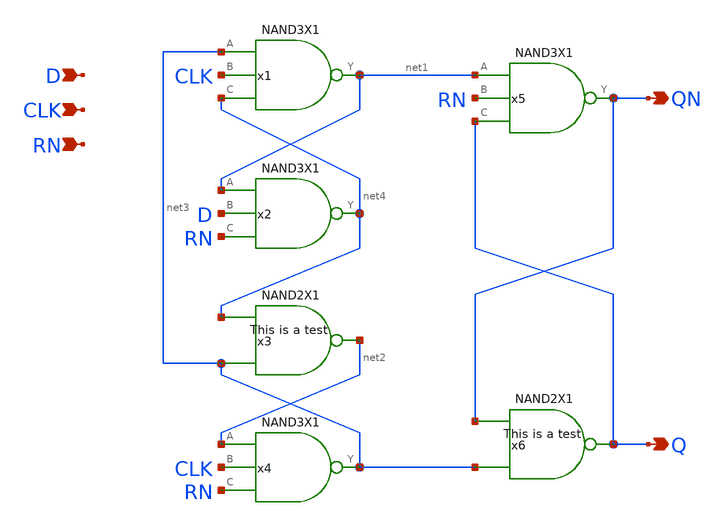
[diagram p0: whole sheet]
** sch_path: archives/lib/xschem/DFFRNX1.sch
**.subckt DFFRNX1 Q QN D CLK RN
*.opin Q
*.opin QN
*.ipin D
*.ipin CLK
*.ipin RN
x2 net4 net1 D RN VDD VSS NAND3X1
x1 net1 net3 CLK net4 VDD VSS NAND3X1
x3 net2 net4 net3 VDD VSS NAND2X1
x4 net3 net2 CLK RN VDD VSS NAND3X1
x5 QN net1 RN Q VDD VSS NAND3X1
x6 Q QN net3 VDD VSS NAND2X1
**.ends
.end
